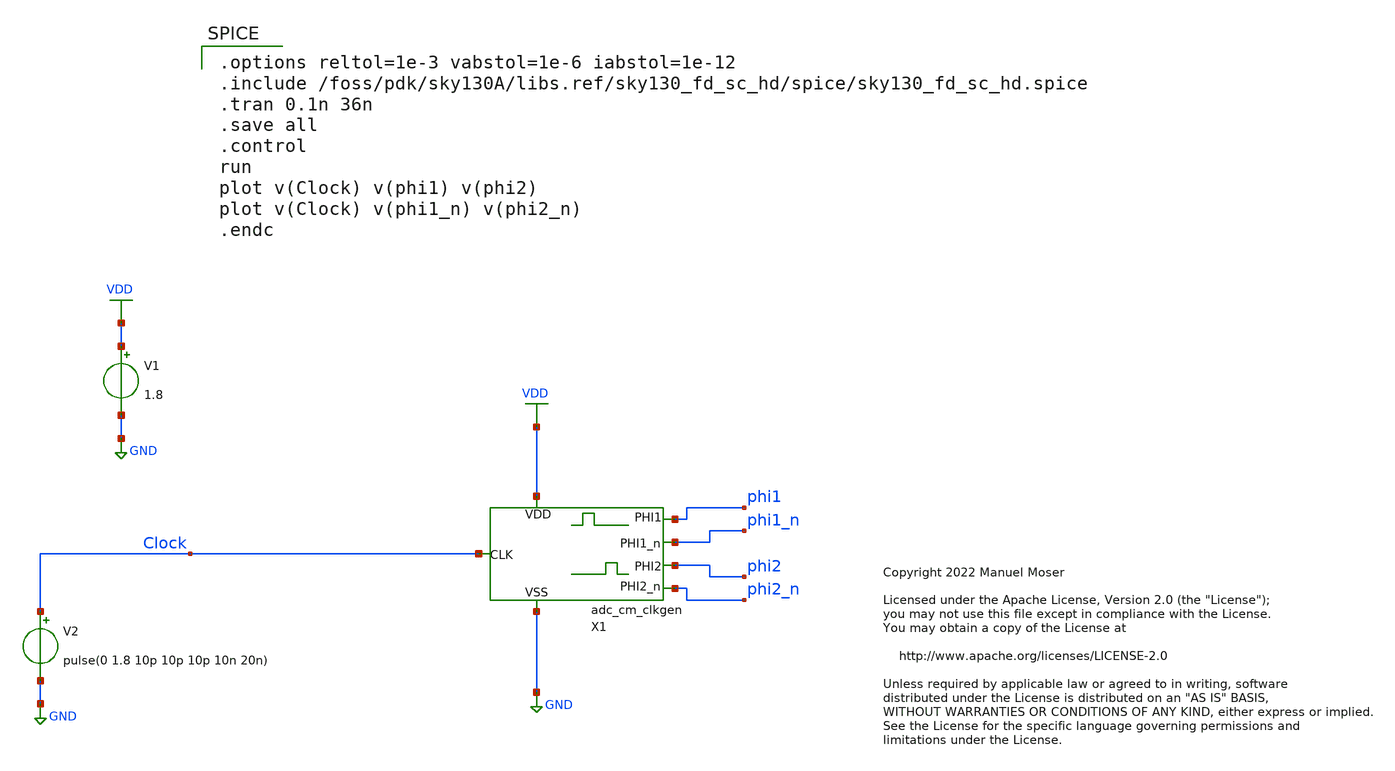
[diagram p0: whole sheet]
** sch_path: xschem/archive/adc_cm_clkgen/analog/adc_cm_clkgen_transient.sch
* Copyright 2022 Manuel Moser
* Licensed under the Apache License, Version 2.0 (the "License");
**.subckt adc_cm_clkgen_transient
V1 VDD GND 1.8
V2 Clock GND pulse(0 1.8 10p 10p 10p 10n 20n)
X1 Clock VDD GND phi1_n phi1 phi2 phi2_n adc_cm_clkgen
**** begin user architecture code

.options reltol=1e-3 vabstol=1e-6 iabstol=1e-12
.include /foss/pdk/sky130A/libs.ref/sky130_fd_sc_hd/spice/sky130_fd_sc_hd.spice
.tran 0.1n 36n
.save all
.control
run
plot v(Clock) v(phi1) v(phi2)
plot v(Clock) v(phi1_n) v(phi2_n)
.endc



** opencircuitdesign pdks install
.lib $::SKYWATER_MODELS/sky130.lib.spice tt


**** end user architecture code
**.ends
.GLOBAL GND
.GLOBAL VDD
.end
